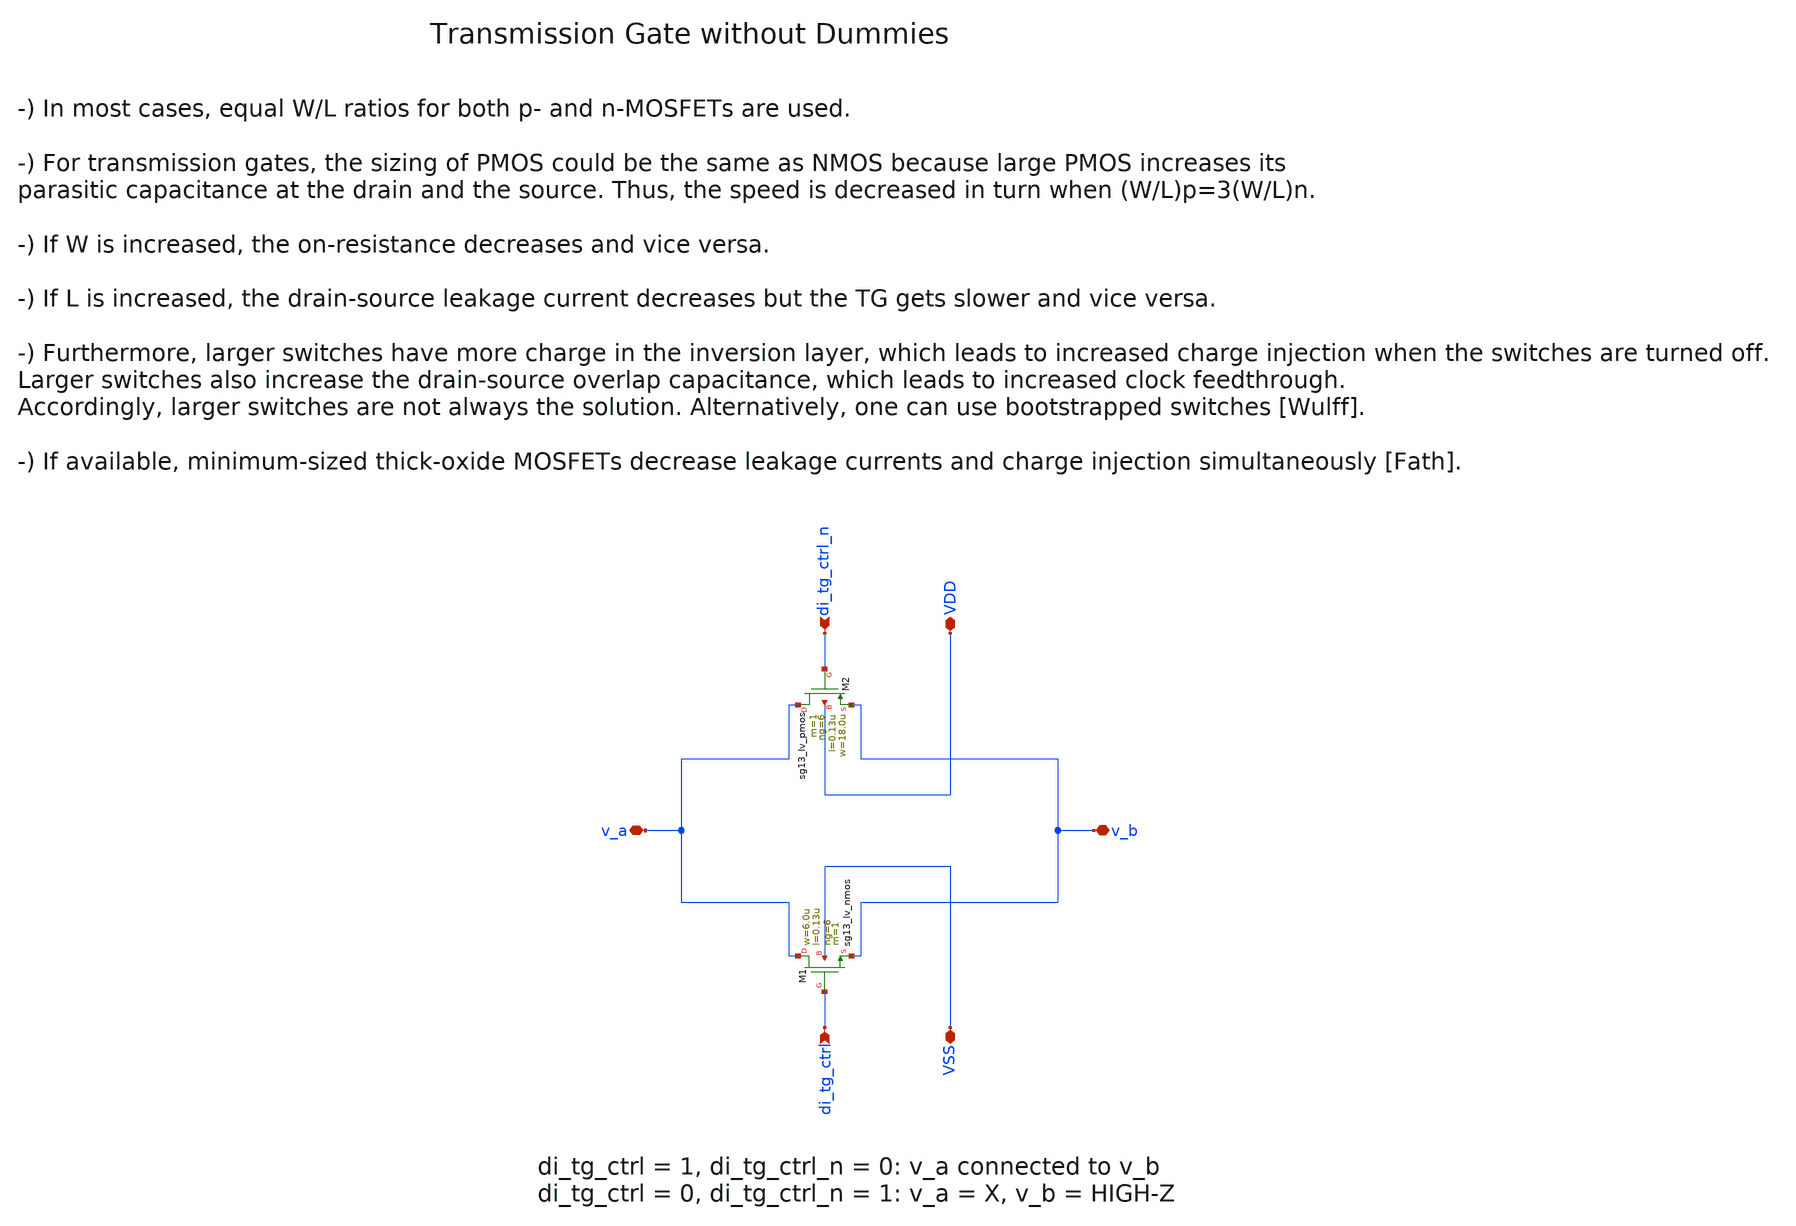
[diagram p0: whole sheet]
** sch_path: ihp130/macros/iqmod/schematic/xschem/iqmod_mixer_se2diff_tg_NF6.sch
**.subckt iqmod_mixer_se2diff_tg_NF6 v_a v_b VDD VSS di_tg_ctrl di_tg_ctrl_n
*.iopin v_a
*.iopin v_b
*.iopin VDD
*.iopin VSS
*.ipin di_tg_ctrl
*.ipin di_tg_ctrl_n
XM2 v_a di_tg_ctrl_n v_b VDD sg13_lv_pmos w=18.0u l=0.13u ng=6 m=1 mm_ok=1
XM1 v_a di_tg_ctrl v_b VSS sg13_lv_nmos w=6.0u l=0.13u ng=6 m=1 mm_ok=1
**.ends
.end
